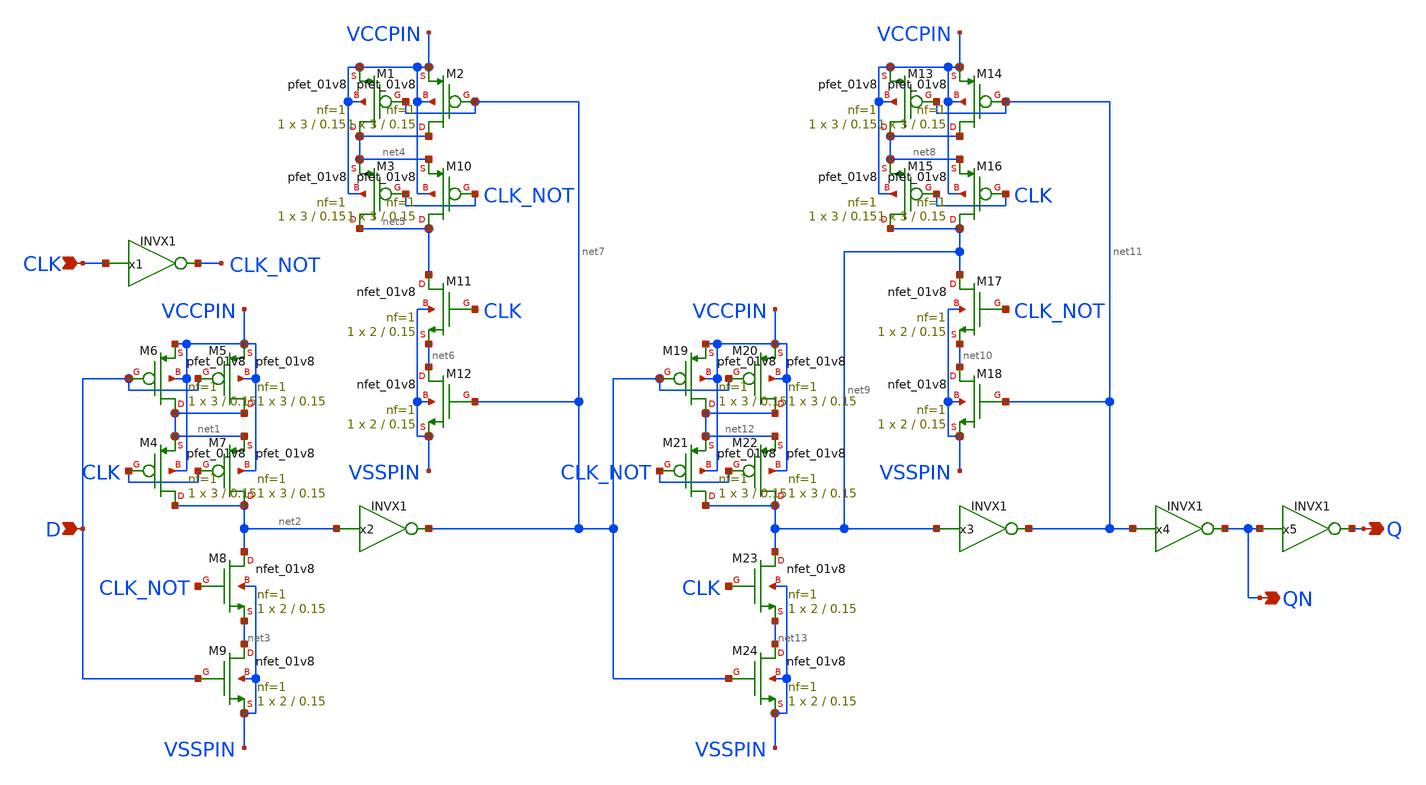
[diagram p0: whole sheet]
** sch_path: lib/xschem/DFFQN.sch
**.subckt DFFQN CLK D Q QN
*.ipin CLK
*.ipin D
*.opin Q
*.opin QN
XM8 net2 CLK_NOT net3 VSSPIN sky130_fd_pr__nfet_01v8 L=0.15 W=2 nf=1 ad='int((nf+1)/2) * W/nf * 0.29'
+ as='int((nf+2)/2) * W/nf * 0.29' pd='2*int((nf+1)/2) * (W/nf + 0.29)' ps='2*int((nf+2)/2) * (W/nf + 0.29)'
+ nrd='0.29 / W' nrs='0.29 / W' sa=0 sb=0 sd=0 mult=1 m=1
XM6 net1 D VCCPIN VCCPIN sky130_fd_pr__pfet_01v8 L=0.15 W=3 nf=1 ad='int((nf+1)/2) * W/nf * 0.29' as='int((nf+2)/2) * W/nf * 0.29'
+ pd='2*int((nf+1)/2) * (W/nf + 0.29)' ps='2*int((nf+2)/2) * (W/nf + 0.29)' nrd='0.29 / W' nrs='0.29 / W'
+ sa=0 sb=0 sd=0 mult=1 m=1
XM9 net3 D VSSPIN VSSPIN sky130_fd_pr__nfet_01v8 L=0.15 W=2 nf=1 ad='int((nf+1)/2) * W/nf * 0.29' as='int((nf+2)/2) * W/nf * 0.29'
+ pd='2*int((nf+1)/2) * (W/nf + 0.29)' ps='2*int((nf+2)/2) * (W/nf + 0.29)' nrd='0.29 / W' nrs='0.29 / W'
+ sa=0 sb=0 sd=0 mult=1 m=1
XM4 net2 CLK net1 VCCPIN sky130_fd_pr__pfet_01v8 L=0.15 W=3 nf=1 ad='int((nf+1)/2) * W/nf * 0.29' as='int((nf+2)/2) * W/nf * 0.29'
+ pd='2*int((nf+1)/2) * (W/nf + 0.29)' ps='2*int((nf+2)/2) * (W/nf + 0.29)' nrd='0.29 / W' nrs='0.29 / W'
+ sa=0 sb=0 sd=0 mult=1 m=1
XM5 net1 D VCCPIN VCCPIN sky130_fd_pr__pfet_01v8 L=0.15 W=3 nf=1 ad='int((nf+1)/2) * W/nf * 0.29' as='int((nf+2)/2) * W/nf * 0.29'
+ pd='2*int((nf+1)/2) * (W/nf + 0.29)' ps='2*int((nf+2)/2) * (W/nf + 0.29)' nrd='0.29 / W' nrs='0.29 / W'
+ sa=0 sb=0 sd=0 mult=1 m=1
XM7 net2 CLK net1 VCCPIN sky130_fd_pr__pfet_01v8 L=0.15 W=3 nf=1 ad='int((nf+1)/2) * W/nf * 0.29' as='int((nf+2)/2) * W/nf * 0.29'
+ pd='2*int((nf+1)/2) * (W/nf + 0.29)' ps='2*int((nf+2)/2) * (W/nf + 0.29)' nrd='0.29 / W' nrs='0.29 / W'
+ sa=0 sb=0 sd=0 mult=1 m=1
XM11 net5 CLK net6 VSSPIN sky130_fd_pr__nfet_01v8 L=0.15 W=2 nf=1 ad='int((nf+1)/2) * W/nf * 0.29' as='int((nf+2)/2) * W/nf * 0.29'
+ pd='2*int((nf+1)/2) * (W/nf + 0.29)' ps='2*int((nf+2)/2) * (W/nf + 0.29)' nrd='0.29 / W' nrs='0.29 / W'
+ sa=0 sb=0 sd=0 mult=1 m=1
XM12 net6 net7 VSSPIN VSSPIN sky130_fd_pr__nfet_01v8 L=0.15 W=2 nf=1 ad='int((nf+1)/2) * W/nf * 0.29'
+ as='int((nf+2)/2) * W/nf * 0.29' pd='2*int((nf+1)/2) * (W/nf + 0.29)' ps='2*int((nf+2)/2) * (W/nf + 0.29)'
+ nrd='0.29 / W' nrs='0.29 / W' sa=0 sb=0 sd=0 mult=1 m=1
XM1 net4 net7 VCCPIN VCCPIN sky130_fd_pr__pfet_01v8 L=0.15 W=3 nf=1 ad='int((nf+1)/2) * W/nf * 0.29'
+ as='int((nf+2)/2) * W/nf * 0.29' pd='2*int((nf+1)/2) * (W/nf + 0.29)' ps='2*int((nf+2)/2) * (W/nf + 0.29)'
+ nrd='0.29 / W' nrs='0.29 / W' sa=0 sb=0 sd=0 mult=1 m=1
XM2 net4 net7 VCCPIN VCCPIN sky130_fd_pr__pfet_01v8 L=0.15 W=3 nf=1 ad='int((nf+1)/2) * W/nf * 0.29'
+ as='int((nf+2)/2) * W/nf * 0.29' pd='2*int((nf+1)/2) * (W/nf + 0.29)' ps='2*int((nf+2)/2) * (W/nf + 0.29)'
+ nrd='0.29 / W' nrs='0.29 / W' sa=0 sb=0 sd=0 mult=1 m=1
XM3 net5 CLK_NOT net4 VCCPIN sky130_fd_pr__pfet_01v8 L=0.15 W=3 nf=1 ad='int((nf+1)/2) * W/nf * 0.29'
+ as='int((nf+2)/2) * W/nf * 0.29' pd='2*int((nf+1)/2) * (W/nf + 0.29)' ps='2*int((nf+2)/2) * (W/nf + 0.29)'
+ nrd='0.29 / W' nrs='0.29 / W' sa=0 sb=0 sd=0 mult=1 m=1
XM10 net5 CLK_NOT net4 VCCPIN sky130_fd_pr__pfet_01v8 L=0.15 W=3 nf=1 ad='int((nf+1)/2) * W/nf * 0.29'
+ as='int((nf+2)/2) * W/nf * 0.29' pd='2*int((nf+1)/2) * (W/nf + 0.29)' ps='2*int((nf+2)/2) * (W/nf + 0.29)'
+ nrd='0.29 / W' nrs='0.29 / W' sa=0 sb=0 sd=0 mult=1 m=1
XM19 net12 net7 VCCPIN VCCPIN sky130_fd_pr__pfet_01v8 L=0.15 W=3 nf=1 ad='int((nf+1)/2) * W/nf * 0.29'
+ as='int((nf+2)/2) * W/nf * 0.29' pd='2*int((nf+1)/2) * (W/nf + 0.29)' ps='2*int((nf+2)/2) * (W/nf + 0.29)'
+ nrd='0.29 / W' nrs='0.29 / W' sa=0 sb=0 sd=0 mult=1 m=1
XM20 net12 net7 VCCPIN VCCPIN sky130_fd_pr__pfet_01v8 L=0.15 W=3 nf=1 ad='int((nf+1)/2) * W/nf * 0.29'
+ as='int((nf+2)/2) * W/nf * 0.29' pd='2*int((nf+1)/2) * (W/nf + 0.29)' ps='2*int((nf+2)/2) * (W/nf + 0.29)'
+ nrd='0.29 / W' nrs='0.29 / W' sa=0 sb=0 sd=0 mult=1 m=1
XM21 net9 CLK_NOT net12 VCCPIN sky130_fd_pr__pfet_01v8 L=0.15 W=3 nf=1 ad='int((nf+1)/2) * W/nf * 0.29'
+ as='int((nf+2)/2) * W/nf * 0.29' pd='2*int((nf+1)/2) * (W/nf + 0.29)' ps='2*int((nf+2)/2) * (W/nf + 0.29)'
+ nrd='0.29 / W' nrs='0.29 / W' sa=0 sb=0 sd=0 mult=1 m=1
XM22 net9 CLK_NOT net12 VCCPIN sky130_fd_pr__pfet_01v8 L=0.15 W=3 nf=1 ad='int((nf+1)/2) * W/nf * 0.29'
+ as='int((nf+2)/2) * W/nf * 0.29' pd='2*int((nf+1)/2) * (W/nf + 0.29)' ps='2*int((nf+2)/2) * (W/nf + 0.29)'
+ nrd='0.29 / W' nrs='0.29 / W' sa=0 sb=0 sd=0 mult=1 m=1
XM23 net9 CLK net13 VSSPIN sky130_fd_pr__nfet_01v8 L=0.15 W=2 nf=1 ad='int((nf+1)/2) * W/nf * 0.29' as='int((nf+2)/2) * W/nf * 0.29'
+ pd='2*int((nf+1)/2) * (W/nf + 0.29)' ps='2*int((nf+2)/2) * (W/nf + 0.29)' nrd='0.29 / W' nrs='0.29 / W'
+ sa=0 sb=0 sd=0 mult=1 m=1
XM24 net13 net7 VSSPIN VSSPIN sky130_fd_pr__nfet_01v8 L=0.15 W=2 nf=1 ad='int((nf+1)/2) * W/nf * 0.29'
+ as='int((nf+2)/2) * W/nf * 0.29' pd='2*int((nf+1)/2) * (W/nf + 0.29)' ps='2*int((nf+2)/2) * (W/nf + 0.29)'
+ nrd='0.29 / W' nrs='0.29 / W' sa=0 sb=0 sd=0 mult=1 m=1
XM13 net8 net11 VCCPIN VCCPIN sky130_fd_pr__pfet_01v8 L=0.15 W=3 nf=1 ad='int((nf+1)/2) * W/nf * 0.29'
+ as='int((nf+2)/2) * W/nf * 0.29' pd='2*int((nf+1)/2) * (W/nf + 0.29)' ps='2*int((nf+2)/2) * (W/nf + 0.29)'
+ nrd='0.29 / W' nrs='0.29 / W' sa=0 sb=0 sd=0 mult=1 m=1
XM14 net8 net11 VCCPIN VCCPIN sky130_fd_pr__pfet_01v8 L=0.15 W=3 nf=1 ad='int((nf+1)/2) * W/nf * 0.29'
+ as='int((nf+2)/2) * W/nf * 0.29' pd='2*int((nf+1)/2) * (W/nf + 0.29)' ps='2*int((nf+2)/2) * (W/nf + 0.29)'
+ nrd='0.29 / W' nrs='0.29 / W' sa=0 sb=0 sd=0 mult=1 m=1
XM15 net9 CLK net8 VCCPIN sky130_fd_pr__pfet_01v8 L=0.15 W=3 nf=1 ad='int((nf+1)/2) * W/nf * 0.29' as='int((nf+2)/2) * W/nf * 0.29'
+ pd='2*int((nf+1)/2) * (W/nf + 0.29)' ps='2*int((nf+2)/2) * (W/nf + 0.29)' nrd='0.29 / W' nrs='0.29 / W'
+ sa=0 sb=0 sd=0 mult=1 m=1
XM16 net9 CLK net8 VCCPIN sky130_fd_pr__pfet_01v8 L=0.15 W=3 nf=1 ad='int((nf+1)/2) * W/nf * 0.29' as='int((nf+2)/2) * W/nf * 0.29'
+ pd='2*int((nf+1)/2) * (W/nf + 0.29)' ps='2*int((nf+2)/2) * (W/nf + 0.29)' nrd='0.29 / W' nrs='0.29 / W'
+ sa=0 sb=0 sd=0 mult=1 m=1
XM17 net9 CLK_NOT net10 VSSPIN sky130_fd_pr__nfet_01v8 L=0.15 W=2 nf=1 ad='int((nf+1)/2) * W/nf * 0.29'
+ as='int((nf+2)/2) * W/nf * 0.29' pd='2*int((nf+1)/2) * (W/nf + 0.29)' ps='2*int((nf+2)/2) * (W/nf + 0.29)'
+ nrd='0.29 / W' nrs='0.29 / W' sa=0 sb=0 sd=0 mult=1 m=1
XM18 net10 net11 VSSPIN VSSPIN sky130_fd_pr__nfet_01v8 L=0.15 W=2 nf=1 ad='int((nf+1)/2) * W/nf * 0.29'
+ as='int((nf+2)/2) * W/nf * 0.29' pd='2*int((nf+1)/2) * (W/nf + 0.29)' ps='2*int((nf+2)/2) * (W/nf + 0.29)'
+ nrd='0.29 / W' nrs='0.29 / W' sa=0 sb=0 sd=0 mult=1 m=1
x1 CLK_NOT CLK VCCPIN VSSPIN INVX1
x2 net7 net2 VCCPIN VSSPIN INVX1
x3 net11 net9 VCCPIN VSSPIN INVX1
x4 QN net11 VCCPIN VSSPIN INVX1
x5 Q QN VCCPIN VSSPIN INVX1
**.ends

* expanding   symbol:  INVX1.sym # of pins=2
** sym_path: lib/xschem/INVX1.sym
** sch_path: lib/xschem/INVX1.sch
.subckt INVX1 Y A VCCPIN VSSPIN
*.ipin A
*.opin Y
XM1 Y A VSSPIN VSSPIN sky130_fd_pr__nfet_01v8 L=0.15 W=3 nf=1 ad='int((nf+1)/2) * W/nf * 0.29' as='int((nf+2)/2) * W/nf * 0.29'
+ pd='2*int((nf+1)/2) * (W/nf + 0.29)' ps='2*int((nf+2)/2) * (W/nf + 0.29)' nrd='0.29 / W' nrs='0.29 / W'
+ sa=0 sb=0 sd=0 mult=1 m=1
XM2 Y A VCCPIN VCCPIN sky130_fd_pr__pfet_01v8 L=0.15 W=2 nf=1 ad='int((nf+1)/2) * W/nf * 0.29' as='int((nf+2)/2) * W/nf * 0.29'
+ pd='2*int((nf+1)/2) * (W/nf + 0.29)' ps='2*int((nf+2)/2) * (W/nf + 0.29)' nrd='0.29 / W' nrs='0.29 / W'
+ sa=0 sb=0 sd=0 mult=1 m=1
XM3 Y A VCCPIN VCCPIN sky130_fd_pr__pfet_01v8 L=0.15 W=2 nf=1 ad='int((nf+1)/2) * W/nf * 0.29' as='int((nf+2)/2) * W/nf * 0.29'
+ pd='2*int((nf+1)/2) * (W/nf + 0.29)' ps='2*int((nf+2)/2) * (W/nf + 0.29)' nrd='0.29 / W' nrs='0.29 / W'
+ sa=0 sb=0 sd=0 mult=1 m=1
.ends

.end
